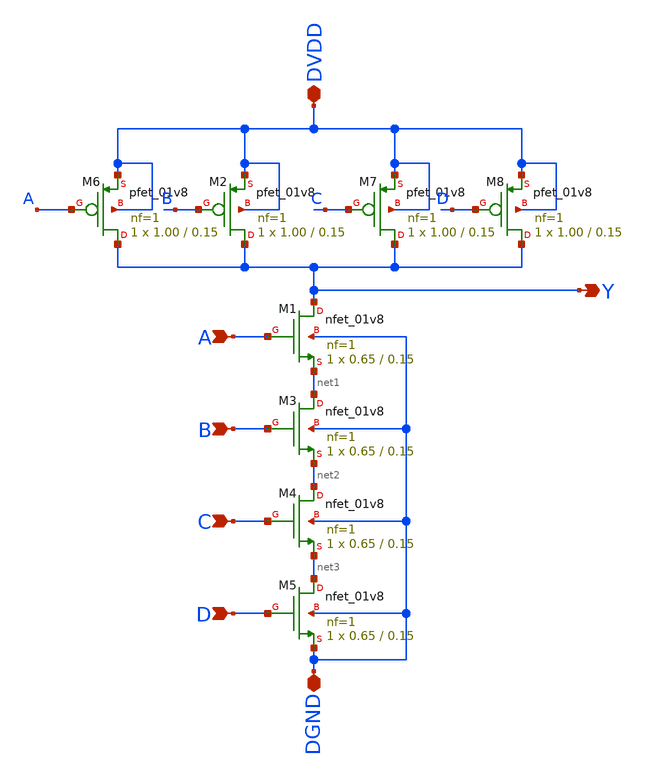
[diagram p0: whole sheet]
** sch_path: project/sch_sym_files/nand4.sch
**.subckt nand4 Y A DVDD DGND B C D
*.opin Y
*.ipin A
*.iopin DVDD
*.iopin DGND
*.ipin B
*.ipin C
*.ipin D
XM2 Y B DVDD DVDD sky130_fd_pr__pfet_01v8 L=0.15 W=1.00 nf=1 ad='int((nf+1)/2) * W/nf * 0.29' as='int((nf+2)/2) * W/nf * 0.29'
+ pd='2*int((nf+1)/2) * (W/nf + 0.29)' ps='2*int((nf+2)/2) * (W/nf + 0.29)' nrd='0.29 / W' nrs='0.29 / W'
+ sa=0 sb=0 sd=0 mult=1 m=1
XM1 Y A net1 DGND sky130_fd_pr__nfet_01v8 L=0.15 W=0.65 nf=1 ad='int((nf+1)/2) * W/nf * 0.29' as='int((nf+2)/2) * W/nf * 0.29'
+ pd='2*int((nf+1)/2) * (W/nf + 0.29)' ps='2*int((nf+2)/2) * (W/nf + 0.29)' nrd='0.29 / W' nrs='0.29 / W'
+ sa=0 sb=0 sd=0 mult=1 m=1
XM3 net1 B net2 DGND sky130_fd_pr__nfet_01v8 L=0.15 W=0.65 nf=1 ad='int((nf+1)/2) * W/nf * 0.29' as='int((nf+2)/2) * W/nf * 0.29'
+ pd='2*int((nf+1)/2) * (W/nf + 0.29)' ps='2*int((nf+2)/2) * (W/nf + 0.29)' nrd='0.29 / W' nrs='0.29 / W'
+ sa=0 sb=0 sd=0 mult=1 m=1
XM4 net2 C net3 DGND sky130_fd_pr__nfet_01v8 L=0.15 W=0.65 nf=1 ad='int((nf+1)/2) * W/nf * 0.29' as='int((nf+2)/2) * W/nf * 0.29'
+ pd='2*int((nf+1)/2) * (W/nf + 0.29)' ps='2*int((nf+2)/2) * (W/nf + 0.29)' nrd='0.29 / W' nrs='0.29 / W'
+ sa=0 sb=0 sd=0 mult=1 m=1
XM5 net3 D DGND DGND sky130_fd_pr__nfet_01v8 L=0.15 W=0.65 nf=1 ad='int((nf+1)/2) * W/nf * 0.29' as='int((nf+2)/2) * W/nf * 0.29'
+ pd='2*int((nf+1)/2) * (W/nf + 0.29)' ps='2*int((nf+2)/2) * (W/nf + 0.29)' nrd='0.29 / W' nrs='0.29 / W'
+ sa=0 sb=0 sd=0 mult=1 m=1
XM6 Y A DVDD DVDD sky130_fd_pr__pfet_01v8 L=0.15 W=1.00 nf=1 ad='int((nf+1)/2) * W/nf * 0.29' as='int((nf+2)/2) * W/nf * 0.29'
+ pd='2*int((nf+1)/2) * (W/nf + 0.29)' ps='2*int((nf+2)/2) * (W/nf + 0.29)' nrd='0.29 / W' nrs='0.29 / W'
+ sa=0 sb=0 sd=0 mult=1 m=1
XM7 Y C DVDD DVDD sky130_fd_pr__pfet_01v8 L=0.15 W=1.00 nf=1 ad='int((nf+1)/2) * W/nf * 0.29' as='int((nf+2)/2) * W/nf * 0.29'
+ pd='2*int((nf+1)/2) * (W/nf + 0.29)' ps='2*int((nf+2)/2) * (W/nf + 0.29)' nrd='0.29 / W' nrs='0.29 / W'
+ sa=0 sb=0 sd=0 mult=1 m=1
XM8 Y D DVDD DVDD sky130_fd_pr__pfet_01v8 L=0.15 W=1.00 nf=1 ad='int((nf+1)/2) * W/nf * 0.29' as='int((nf+2)/2) * W/nf * 0.29'
+ pd='2*int((nf+1)/2) * (W/nf + 0.29)' ps='2*int((nf+2)/2) * (W/nf + 0.29)' nrd='0.29 / W' nrs='0.29 / W'
+ sa=0 sb=0 sd=0 mult=1 m=1
**.ends
.end
